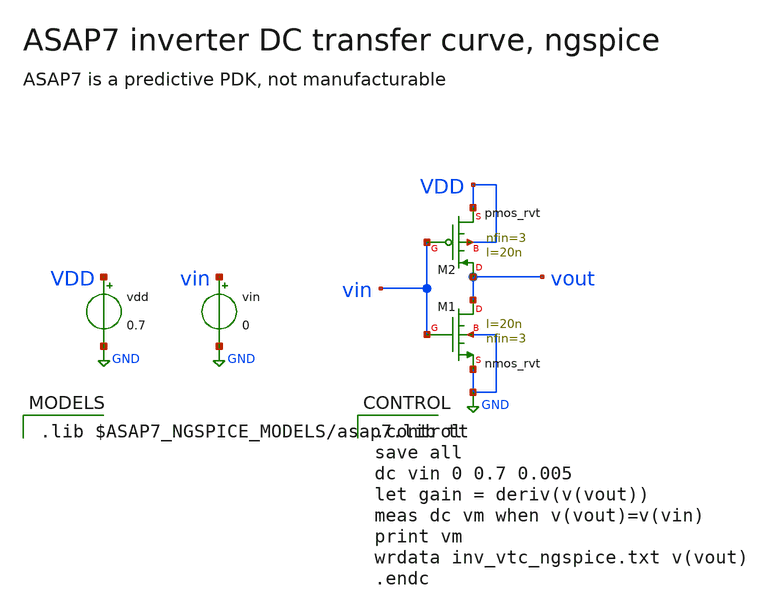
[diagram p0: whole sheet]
** sch_path: _build/images/open_pdks/asap7/libs.tech/xschem/asap7_tests/inv_vtc_ngspice.sch
* SPDX-FileCopyrightText: 2026 Harald Pretl
* Johannes Kepler University, Department for Integrated Circuits
* SPDX-License-Identifier: Apache-2.0
**.subckt inv_vtc_ngspice
XM2 vout vin VDD VDD pmos_rvt l=20n nfin=3
XM1 vout vin GND GND nmos_rvt l=20n nfin=3
vdd VDD GND 0.7
vin vin GND 0
**** begin user architecture code

.lib $ASAP7_NGSPICE_MODELS/asap7.lib tt



.control
save all
dc vin 0 0.7 0.005
let gain = deriv(v(vout))
meas dc vm when v(vout)=v(vin)
print vm
wrdata inv_vtc_ngspice.txt v(vout)
.endc


**** end user architecture code
**.ends
.GLOBAL GND
.end
